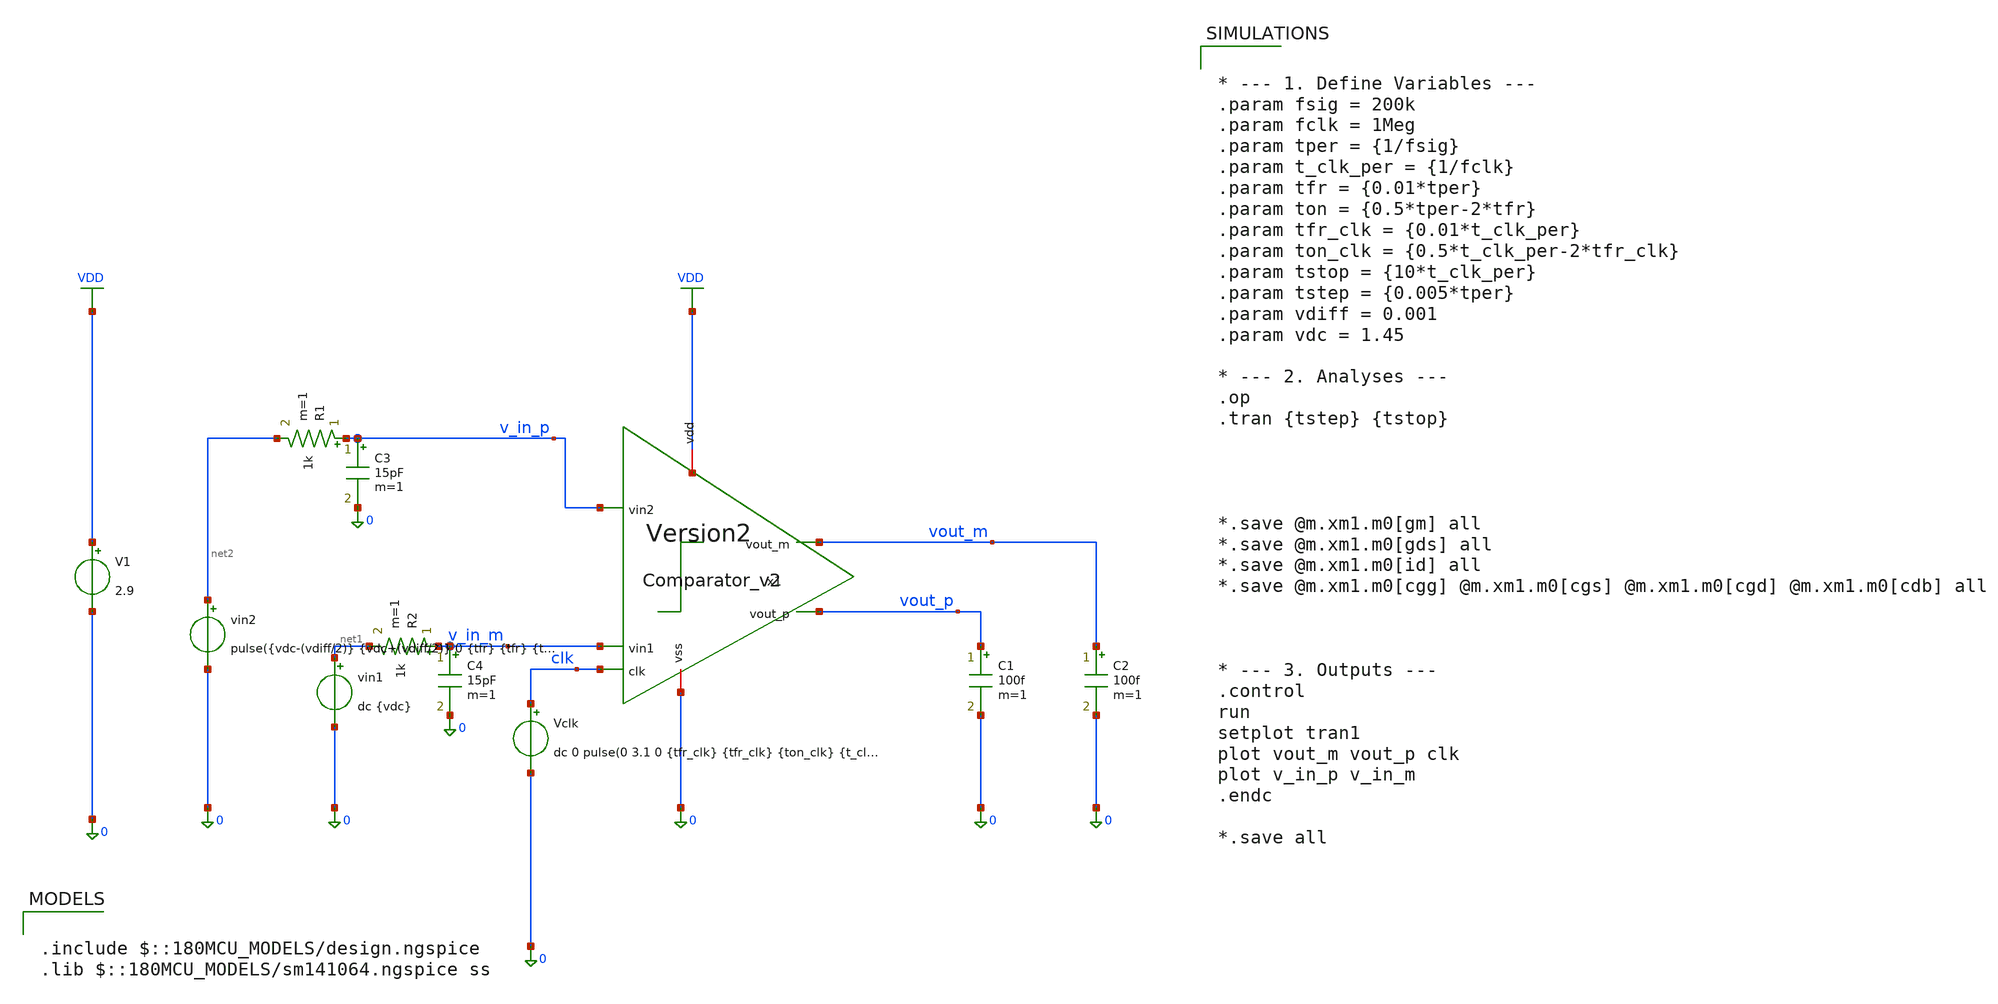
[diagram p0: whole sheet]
** sch_path: Felix/Comparator_tb2.sch
**.subckt Comparator_tb2
V1 VDD 0 2.9
vin2 net2 0 pulse({vdc-(vdiff/2)} {vdc+(vdiff/2)} 0 {tfr} {tfr} {ton} {tper})
vin1 net1 0 dc {vdc}
Vclk clk 0 dc 0 pulse(0 3.1 0 {tfr_clk} {tfr_clk} {ton_clk} {t_clk_per})
C1 vout_p 0 100f m=1
C2 vout_m 0 100f m=1
x1 VDD vout_m vout_p v_in_p v_in_m clk 0 Comparator_v2
R1 v_in_p net2 1k m=1
C3 v_in_p 0 15pF m=1
R2 v_in_m net1 1k m=1
C4 v_in_m 0 15pF m=1
**** begin user architecture code


* --- 1. Define Variables ---
.param fsig = 200k
.param fclk = 1Meg
.param tper = {1/fsig}
.param t_clk_per = {1/fclk}
.param tfr = {0.01*tper}
.param ton = {0.5*tper-2*tfr}
.param tfr_clk = {0.01*t_clk_per}
.param ton_clk = {0.5*t_clk_per-2*tfr_clk}
.param tstop = {10*t_clk_per}
.param tstep = {0.005*tper}
.param vdiff = 0.001
.param vdc = 1.45

* --- 2. Analyses ---
.op
.tran {tstep} {tstop}




*.save @m.xm1.m0[gm] all
*.save @m.xm1.m0[gds] all
*.save @m.xm1.m0[id] all
*.save @m.xm1.m0[cgg] @m.xm1.m0[cgs] @m.xm1.m0[cgd] @m.xm1.m0[cdb] all



* --- 3. Outputs ---
.control
run
setplot tran1
plot vout_m vout_p clk
plot v_in_p v_in_m
.endc

*.save all



.include $::180MCU_MODELS/design.ngspice
.lib $::180MCU_MODELS/sm141064.ngspice ss

**** end user architecture code
**.ends
.GLOBAL VDD
.end
